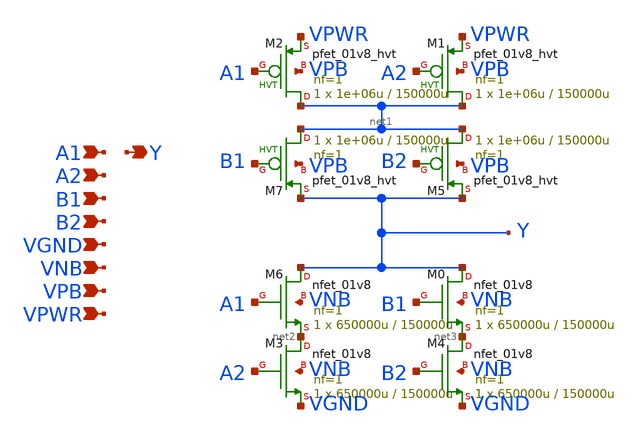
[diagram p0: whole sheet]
** sch_path: schematics/a22oi/sky130_fd_sc_hd__a22oi_1.sch
**.subckt sky130_fd_sc_hd__a22oi_1 A1 A2 B1 B2 VGND VNB VPB VPWR Y
*.ipin A1
*.ipin A2
*.ipin B1
*.ipin B2
*.ipin VGND
*.ipin VNB
*.ipin VPB
*.ipin VPWR
*.opin Y
XM2 net1 A1 VPWR VPB sky130_fd_pr__pfet_01v8_hvt L=150000u W=1e+06u nf=1 ad='int((1 + 1)/2) * 1e+06u / 1 * 0.29'
+ as='int((1 + 2)/2) * 1e+06u / 1 * 0.29' pd='2*int((1 + 1)/2) * (1e+06u / 1 + 0.29)' ps='2*int((1 + 2)/2) * (1e+06u / 1 + 0.29)'
+ nrd='0.29 / 1e+06u ' nrs='0.29 / 1e+06u ' sa=0 sb=0 sd=0 mult=1 m=1
XM1 net1 A2 VPWR VPB sky130_fd_pr__pfet_01v8_hvt L=150000u W=1e+06u nf=1 ad='int((1 + 1)/2) * 1e+06u / 1 * 0.29'
+ as='int((1 + 2)/2) * 1e+06u / 1 * 0.29' pd='2*int((1 + 1)/2) * (1e+06u / 1 + 0.29)' ps='2*int((1 + 2)/2) * (1e+06u / 1 + 0.29)'
+ nrd='0.29 / 1e+06u ' nrs='0.29 / 1e+06u ' sa=0 sb=0 sd=0 mult=1 m=1
XM7 net1 B1 Y VPB sky130_fd_pr__pfet_01v8_hvt L=150000u W=1e+06u nf=1 ad='int((1 + 1)/2) * 1e+06u / 1 * 0.29'
+ as='int((1 + 2)/2) * 1e+06u / 1 * 0.29' pd='2*int((1 + 1)/2) * (1e+06u / 1 + 0.29)' ps='2*int((1 + 2)/2) * (1e+06u / 1 + 0.29)'
+ nrd='0.29 / 1e+06u ' nrs='0.29 / 1e+06u ' sa=0 sb=0 sd=0 mult=1 m=1
XM5 net1 B2 Y VPB sky130_fd_pr__pfet_01v8_hvt L=150000u W=1e+06u nf=1 ad='int((1 + 1)/2) * 1e+06u / 1 * 0.29'
+ as='int((1 + 2)/2) * 1e+06u / 1 * 0.29' pd='2*int((1 + 1)/2) * (1e+06u / 1 + 0.29)' ps='2*int((1 + 2)/2) * (1e+06u / 1 + 0.29)'
+ nrd='0.29 / 1e+06u ' nrs='0.29 / 1e+06u ' sa=0 sb=0 sd=0 mult=1 m=1
XM6 Y A1 net2 VNB sky130_fd_pr__nfet_01v8 L=150000u W=650000u nf=1 ad='int((1 + 1)/2) * 650000u / 1 * 0.29'
+ as='int((1 + 2)/2) * 650000u / 1 * 0.29' pd='2*int((1 + 1)/2) * (650000u / 1 + 0.29)' ps='2*int((1 + 2)/2) * (650000u / 1 + 0.29)'
+ nrd='0.29 / 650000u ' nrs='0.29 / 650000u ' sa=0 sb=0 sd=0 mult=1 m=1
XM3 net2 A2 VGND VNB sky130_fd_pr__nfet_01v8 L=150000u W=650000u nf=1 ad='int((1 + 1)/2) * 650000u / 1 * 0.29'
+ as='int((1 + 2)/2) * 650000u / 1 * 0.29' pd='2*int((1 + 1)/2) * (650000u / 1 + 0.29)' ps='2*int((1 + 2)/2) * (650000u / 1 + 0.29)'
+ nrd='0.29 / 650000u ' nrs='0.29 / 650000u ' sa=0 sb=0 sd=0 mult=1 m=1
XM0 Y B1 net3 VNB sky130_fd_pr__nfet_01v8 L=150000u W=650000u nf=1 ad='int((1 + 1)/2) * 650000u / 1 * 0.29'
+ as='int((1 + 2)/2) * 650000u / 1 * 0.29' pd='2*int((1 + 1)/2) * (650000u / 1 + 0.29)' ps='2*int((1 + 2)/2) * (650000u / 1 + 0.29)'
+ nrd='0.29 / 650000u ' nrs='0.29 / 650000u ' sa=0 sb=0 sd=0 mult=1 m=1
XM4 net3 B2 VGND VNB sky130_fd_pr__nfet_01v8 L=150000u W=650000u nf=1 ad='int((1 + 1)/2) * 650000u / 1 * 0.29'
+ as='int((1 + 2)/2) * 650000u / 1 * 0.29' pd='2*int((1 + 1)/2) * (650000u / 1 + 0.29)' ps='2*int((1 + 2)/2) * (650000u / 1 + 0.29)'
+ nrd='0.29 / 650000u ' nrs='0.29 / 650000u ' sa=0 sb=0 sd=0 mult=1 m=1
**.ends
.end
